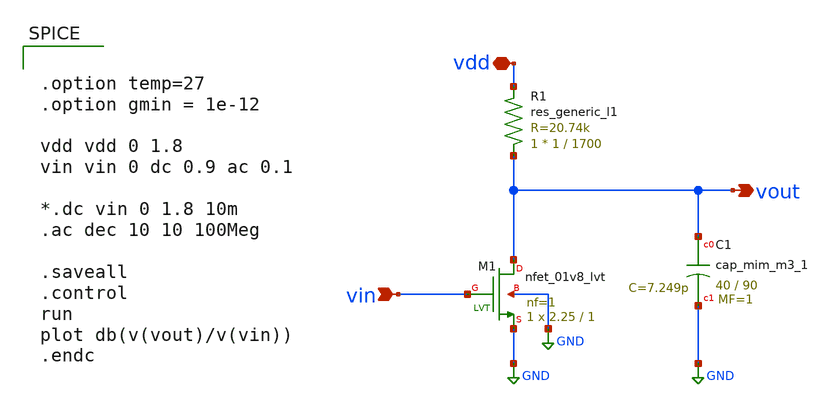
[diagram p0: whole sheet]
** sch_path: src/CS_Resistor.sch
**.subckt CS_Resistor vin vout vdd
*.ipin vin
*.opin vout
*.iopin vdd
R1 vout vdd sky130_fd_pr__res_generic_l1 W=1 L=1700 m=1
XC1 vout GND sky130_fd_pr__cap_mim_m3_1 W=40 L=90 MF=1 m=1
XM1 vout vin GND GND sky130_fd_pr__nfet_01v8_lvt L=1 W=2.25 nf=1 ad='int((nf+1)/2) * W/nf * 0.29' as='int((nf+2)/2) * W/nf * 0.29'
+ pd='2*int((nf+1)/2) * (W/nf + 0.29)' ps='2*int((nf+2)/2) * (W/nf + 0.29)' nrd='0.29 / W' nrs='0.29 / W'
+ sa=0 sb=0 sd=0 mult=1 m=1
**** begin user architecture code

** opencircuitdesign pdks install
.lib $::SKYWATER_MODELS/sky130.lib.spice tt




.option temp=27
.option gmin = 1e-12

vdd vdd 0 1.8
vin vin 0 dc 0.9 ac 0.1

*.dc vin 0 1.8 10m
.ac dec 10 10 100Meg

.saveall
.control
run
plot db(v(vout)/v(vin))
.endc


**** end user architecture code
**.ends
.GLOBAL GND
.end
